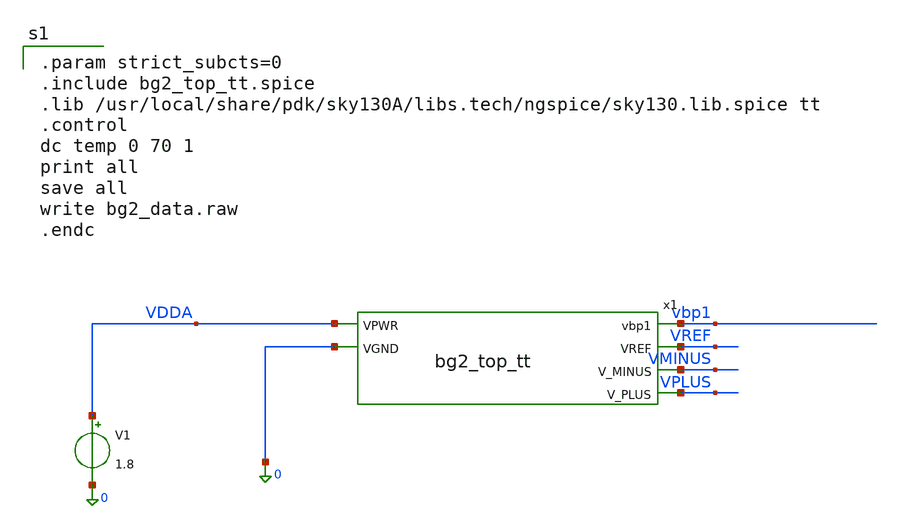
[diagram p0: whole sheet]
** sch_path: lef/lef/lef/gds/bg2_top_tt_tb.sch
**.subckt bg2_top_tt_tb
V1 VDDA 0 1.8
x1 VDDA vbp1 VREF VMINUS VPLUS 0 bg2_top_tt
**** begin user architecture code

.param strict_subcts=0
.include bg2_top_tt.spice
.lib /usr/local/share/pdk/sky130A/libs.tech/ngspice/sky130.lib.spice tt
.control
dc temp 0 70 1
print all
save all
write bg2_data.raw
.endc

**** end user architecture code
**.ends
.end
